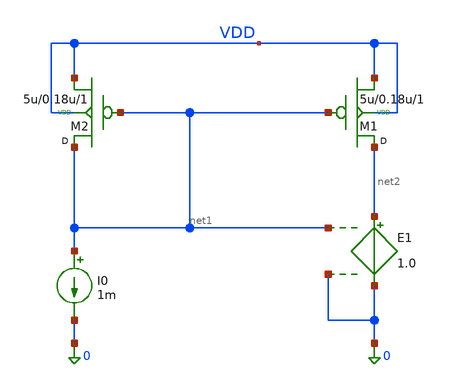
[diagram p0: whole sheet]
** sch_path: lab_2/untitled.sch
**.subckt untitled
M1 net2 net1 VDD VDD pmos w=5u l=0.18u m=1
M2 net1 net1 VDD VDD pmos w=5u l=0.18u m=1
I0 net1 0 1m
E1 net2 0 net1 0 1.0
**.ends
.end
